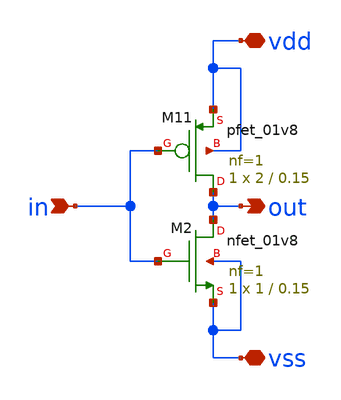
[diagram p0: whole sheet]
** sch_path: xschem/symbols/sky130A_01v8_inv1.sch
* Copyright 2021 Stefan Frederik Schippers
* Licensed under the Apache License, Version 2.0 (the "License");
* you may not use this file except in compliance with the License.
* You may obtain a copy of the License at
* https://www.apache.org/licenses/LICENSE-2.0
* Unless required by applicable law or agreed to in writing, software
* distributed under the License is distributed on an "AS IS" BASIS,
* WITHOUT WARRANTIES OR CONDITIONS OF ANY KIND, either express or implied.
* See the License for the specific language governing permissions and
* limitations under the License.
**.subckt sky130A_01v8_inv1 vdd vss in out
*.iopin vdd
*.iopin vss
*.ipin in
*.opin out
XM11 out in vdd vdd sky130_fd_pr__pfet_01v8 L=0.15 W=2 nf=1 ad='int((nf+1)/2) * W/nf * 0.29' as='int((nf+2)/2) * W/nf * 0.29'
+ pd='2*int((nf+1)/2) * (W/nf + 0.29)' ps='2*int((nf+2)/2) * (W/nf + 0.29)' nrd='0.29 / W' nrs='0.29 / W'
+ sa=0 sb=0 sd=0 mult=1 m=1
XM2 out in vss vss sky130_fd_pr__nfet_01v8 L=0.15 W=1 nf=1 ad='int((1 + 1)/2) * 1 / 1 * 0.29' as='int((1 + 2)/2) * 1 / 1 * 0.29'
+ pd='2*int((1 + 1)/2) * (1 / 1 + 0.29)' ps='2*int((1 + 2)/2) * (1 / 1 + 0.29)' nrd='0.29 / 1 ' nrs='0.29 / 1 '
+ sa=0 sb=0 sd=0 mult=1 m=1
**.ends
.end
